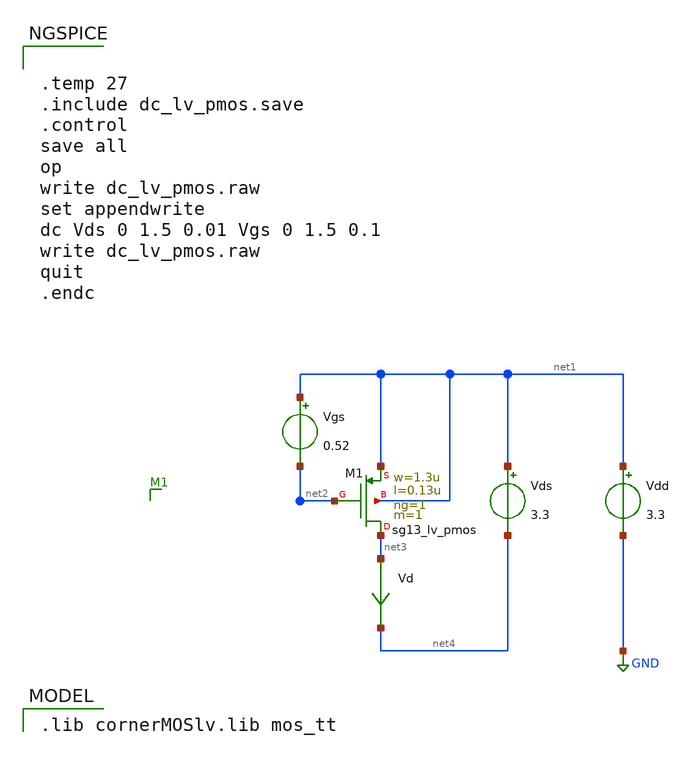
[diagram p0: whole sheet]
** sch_path: xschem/dc_lv_pmos.sch
* (c) 2023-2025 Harald Pretl, Apache-2.0 license
**.subckt dc_lv_pmos
Vgs net1 net2 0.52
Vds net1 net4 3.3
Vd net3 net4 0
.save i(vd)
XM1 net3 net2 net1 net1 sg13_lv_pmos w=1.3u l=0.13u ng=1 m=1 mm_ok=1
Vdd net1 GND 3.3
**** begin user architecture code
 .lib cornerMOSlv.lib mos_tt



.temp 27
.include dc_lv_pmos.save
.control
save all
op
write dc_lv_pmos.raw
set appendwrite
dc Vds 0 1.5 0.01 Vgs 0 1.5 0.1
write dc_lv_pmos.raw
quit
.endc


**** end user architecture code
**.ends
.GLOBAL GND
.end
